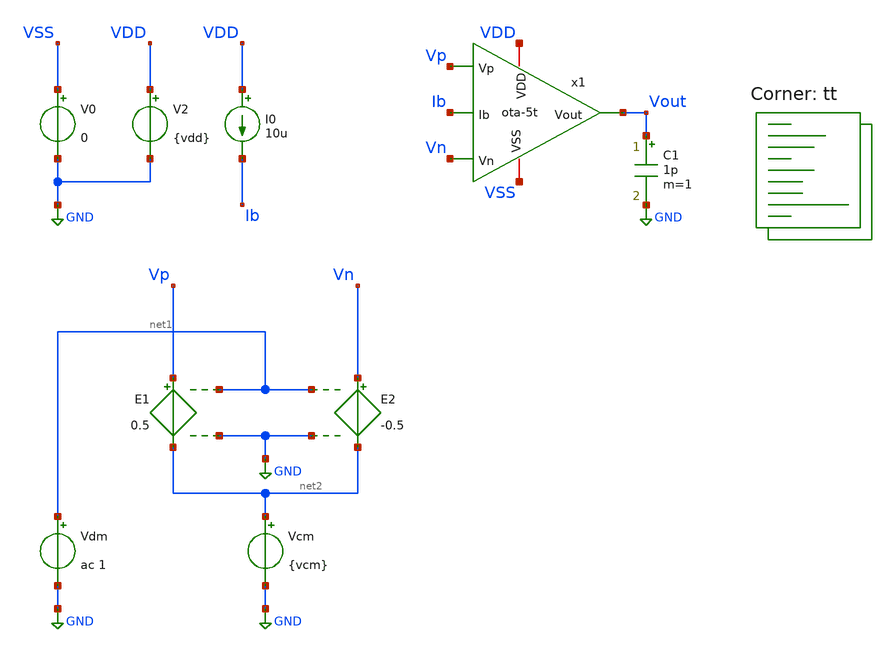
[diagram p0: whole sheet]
** sch_path: xschem/ota-5t_tb.sch
**.subckt ota-5t_tb
I0 VDD Ib 10u
C1 Vout GND 1p m=1
x1 Vp Vn Vout VDD VSS Ib ota-5t
V0 VSS GND 0
V2 VDD GND {vdd}
E1 Vp net2 net1 GND 0.5
E2 Vn net2 net1 GND -0.5
Vdm net1 GND ac 1
Vcm net2 GND {vcm}
**** begin user architecture code


.param vdd=1.8
.param vcm=0.9

.control

    save all

    save @m.x1.xm1.msky130_fd_pr__pfet_01v8[id] @m.x1.xm1.msky130_fd_pr__pfet_01v8[gm]
+ @m.x1.xm1.msky130_fd_pr__pfet_01v8[gds]
    save @m.x1.xm2.msky130_fd_pr__pfet_01v8[id] @m.x1.xm2.msky130_fd_pr__pfet_01v8[gm]
+ @m.x1.xm2.msky130_fd_pr__pfet_01v8[gds]

    save @m.x1.xm3.msky130_fd_pr__nfet_01v8[id] @m.x1.xm3.msky130_fd_pr__nfet_01v8[gm]
+ @m.x1.xm3.msky130_fd_pr__nfet_01v8[gds]
    save @m.x1.xm4.msky130_fd_pr__nfet_01v8[id] @m.x1.xm4.msky130_fd_pr__nfet_01v8[gm]
+ @m.x1.xm4.msky130_fd_pr__nfet_01v8[gds]
    save @m.x1.xm5.msky130_fd_pr__nfet_01v8[id] @m.x1.xm5.msky130_fd_pr__nfet_01v8[gm]
+ @m.x1.xm5.msky130_fd_pr__nfet_01v8[gds]
    save @m.x1.xm6.msky130_fd_pr__nfet_01v8[id] @m.x1.xm6.msky130_fd_pr__nfet_01v8[gm]
+ @m.x1.xm6.msky130_fd_pr__nfet_01v8[gds]

    * operating point
    op

    write ota-5t_tb.raw
    set appendwrite

    * run ac simulation
    ac dec 20 1k 100e6

    * measure parameters
    let vout_mag = abs(v(Vout))
    let vout_phase_margin = phase(v(Vout)) * 180/pi + 180
    meas ac A0 find vout_mag at=1k
    meas ac UGF when vout_mag=1 fall=1
    meas ac PM find vout_phase_margin when vout_mag=1

    write ota-5t_tb.raw
.endc


.lib $::SKYWATER_MODELS/sky130.lib.spice tt
**** end user architecture code
**.ends
.GLOBAL GND
.end
